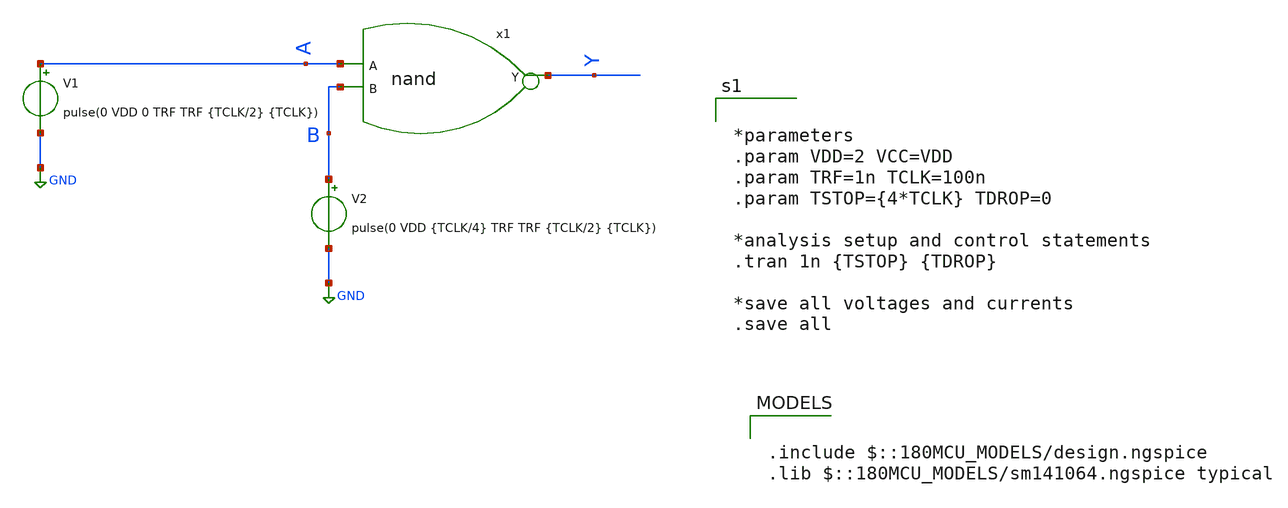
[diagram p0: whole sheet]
** sch_path: XSCHEM Files/nand_tb.sch
**.subckt nand_tb
V1 A GND pulse(0 VDD 0 TRF TRF {TCLK/2} {TCLK})
V2 B GND pulse(0 VDD {TCLK/4} TRF TRF {TCLK/2} {TCLK})
x1 Y A B nand
**** begin user architecture code


*parameters
.param VDD=2 VCC=VDD
.param TRF=1n TCLK=100n
.param TSTOP={4*TCLK} TDROP=0

*analysis setup and control statements
.tran 1n {TSTOP} {TDROP}

*save all voltages and currents
.save all



.include $::180MCU_MODELS/design.ngspice
.lib $::180MCU_MODELS/sm141064.ngspice typical

**** end user architecture code
**.ends

* expanding   symbol:  /home/tare/Desktop/Final/nand.sym # of pins=3
** sym_path: XSCHEM Files/nand.sym
** sch_path: XSCHEM Files/nand.sch
.subckt nand Y A B
*.ipin A
*.opin Y
*.ipin B
**** begin user architecture code


*nand model
a1 [A b] Yi my_nand
.model my_nand d_nand(rise_delay = 1e-9 fall_delay = 1e-9                         input_load =
+ 1e-12)

*force netlisting of digital outputs
v1 Yi Y 0


**** end user architecture code
.ends

.GLOBAL GND
.end
